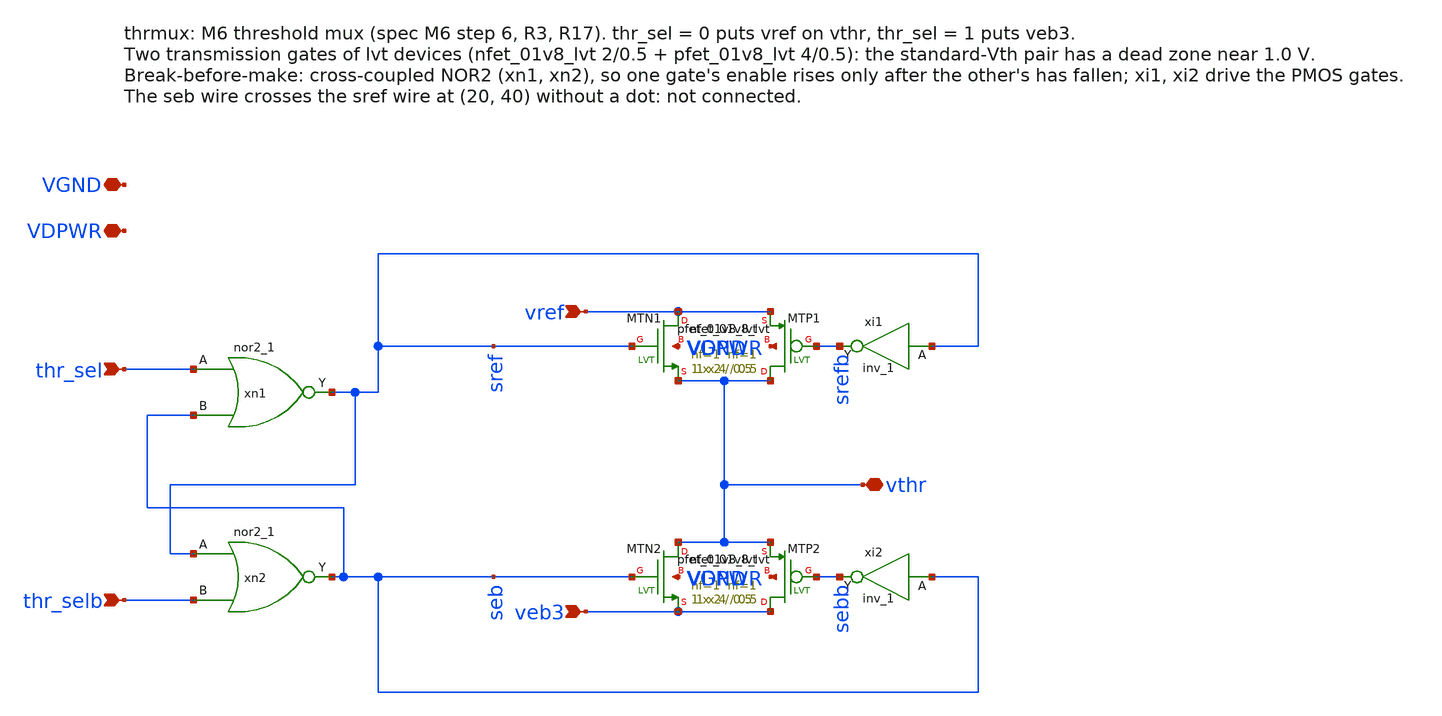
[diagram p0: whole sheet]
** sch_path: xschem/thrmux.sch
**.subckt thrmux thr_sel thr_selb vref veb3 vthr VDPWR VGND
*.ipin thr_sel
*.ipin thr_selb
*.ipin vref
*.ipin veb3
*.iopin vthr
*.iopin VDPWR
*.iopin VGND
xn1 thr_sel seb VGND VGND VDPWR VDPWR sref sky130_fd_sc_hd__nor2_1
xn2 sref thr_selb VGND VGND VDPWR VDPWR seb sky130_fd_sc_hd__nor2_1
xi1 sref VGND VGND VDPWR VDPWR srefb sky130_fd_sc_hd__inv_1
xi2 seb VGND VGND VDPWR VDPWR sebb sky130_fd_sc_hd__inv_1
XMTN1 vref sref vthr VGND sky130_fd_pr__nfet_01v8_lvt L=0.5 W=2 nf=1 ad='int((1 + 1)/2) * 2 / 1 * 0.29'
+ as='int((1 + 2)/2) * 2 / 1 * 0.29' pd='2*int((1 + 1)/2) * (2 / 1 + 0.29)' ps='2*int((1 + 2)/2) * (2 / 1 + 0.29)'
+ nrd='0.29 / 2 ' nrs='0.29 / 2 ' sa=0 sb=0 sd=0 mult=1 m=1
XMTP1 vthr srefb vref VDPWR sky130_fd_pr__pfet_01v8_lvt L=0.5 W=4 nf=1 ad='int((1 + 1)/2) * 4 / 1 * 0.29'
+ as='int((1 + 2)/2) * 4 / 1 * 0.29' pd='2*int((1 + 1)/2) * (4 / 1 + 0.29)' ps='2*int((1 + 2)/2) * (4 / 1 + 0.29)'
+ nrd='0.29 / 4 ' nrs='0.29 / 4 ' sa=0 sb=0 sd=0 mult=1 m=1
XMTN2 vthr seb veb3 VGND sky130_fd_pr__nfet_01v8_lvt L=0.5 W=2 nf=1 ad='int((1 + 1)/2) * 2 / 1 * 0.29'
+ as='int((1 + 2)/2) * 2 / 1 * 0.29' pd='2*int((1 + 1)/2) * (2 / 1 + 0.29)' ps='2*int((1 + 2)/2) * (2 / 1 + 0.29)'
+ nrd='0.29 / 2 ' nrs='0.29 / 2 ' sa=0 sb=0 sd=0 mult=1 m=1
XMTP2 veb3 sebb vthr VDPWR sky130_fd_pr__pfet_01v8_lvt L=0.5 W=4 nf=1 ad='int((1 + 1)/2) * 4 / 1 * 0.29'
+ as='int((1 + 2)/2) * 4 / 1 * 0.29' pd='2*int((1 + 1)/2) * (4 / 1 + 0.29)' ps='2*int((1 + 2)/2) * (4 / 1 + 0.29)'
+ nrd='0.29 / 4 ' nrs='0.29 / 4 ' sa=0 sb=0 sd=0 mult=1 m=1
**.ends
.end
